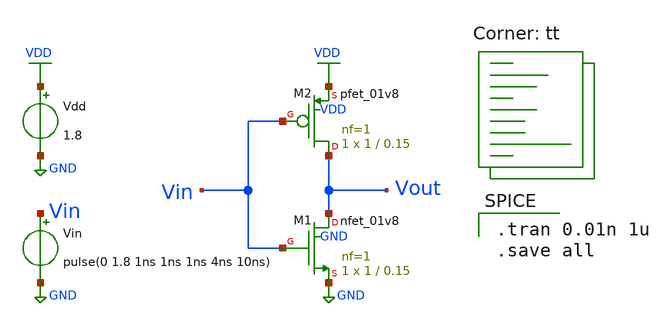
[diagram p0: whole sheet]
** sch_path: inverter_tran.sch
**.subckt inverter_tran
Vdd VDD GND 1.8
XM1 Vout Vin GND GND sky130_fd_pr__nfet_01v8 L=0.15 W=1 nf=1 ad='int((nf+1)/2) * W/nf * 0.29' as='int((nf+2)/2) * W/nf * 0.29'
+ pd='2*int((nf+1)/2) * (W/nf + 0.29)' ps='2*int((nf+2)/2) * (W/nf + 0.29)' nrd='0.29 / W' nrs='0.29 / W'
+ sa=0 sb=0 sd=0 mult=1 m=1
XM2 Vout Vin VDD VDD sky130_fd_pr__pfet_01v8 L=0.15 W=1 nf=1 ad='int((nf+1)/2) * W/nf * 0.29' as='int((nf+2)/2) * W/nf * 0.29'
+ pd='2*int((nf+1)/2) * (W/nf + 0.29)' ps='2*int((nf+2)/2) * (W/nf + 0.29)' nrd='0.29 / W' nrs='0.29 / W'
+ sa=0 sb=0 sd=0 mult=1 m=1
Vin Vin GND pulse(0 1.8 1ns 1ns 1ns 4ns 10ns)
**** begin user architecture code

.tran 0.01n 1u
.save all

.lib $::SKYWATER_MODELS/sky130.lib.spice tt
**** end user architecture code
**.ends
.GLOBAL VDD
.GLOBAL GND
.end
